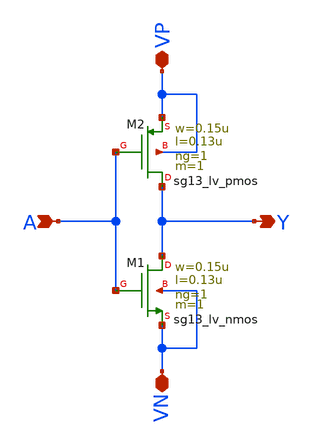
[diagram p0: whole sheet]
** sch_path: inverter/xschem/inverter.sch
**.subckt inverter VP VN A Y
*.iopin VP
*.iopin VN
*.ipin A
*.opin Y
XM1 Y A VN VN sg13_lv_nmos w=0.15u l=0.13u ng=1 m=1 mm_ok=1
XM2 Y A VP VP sg13_lv_pmos w=0.15u l=0.13u ng=1 m=1 mm_ok=1
**.ends
.end
